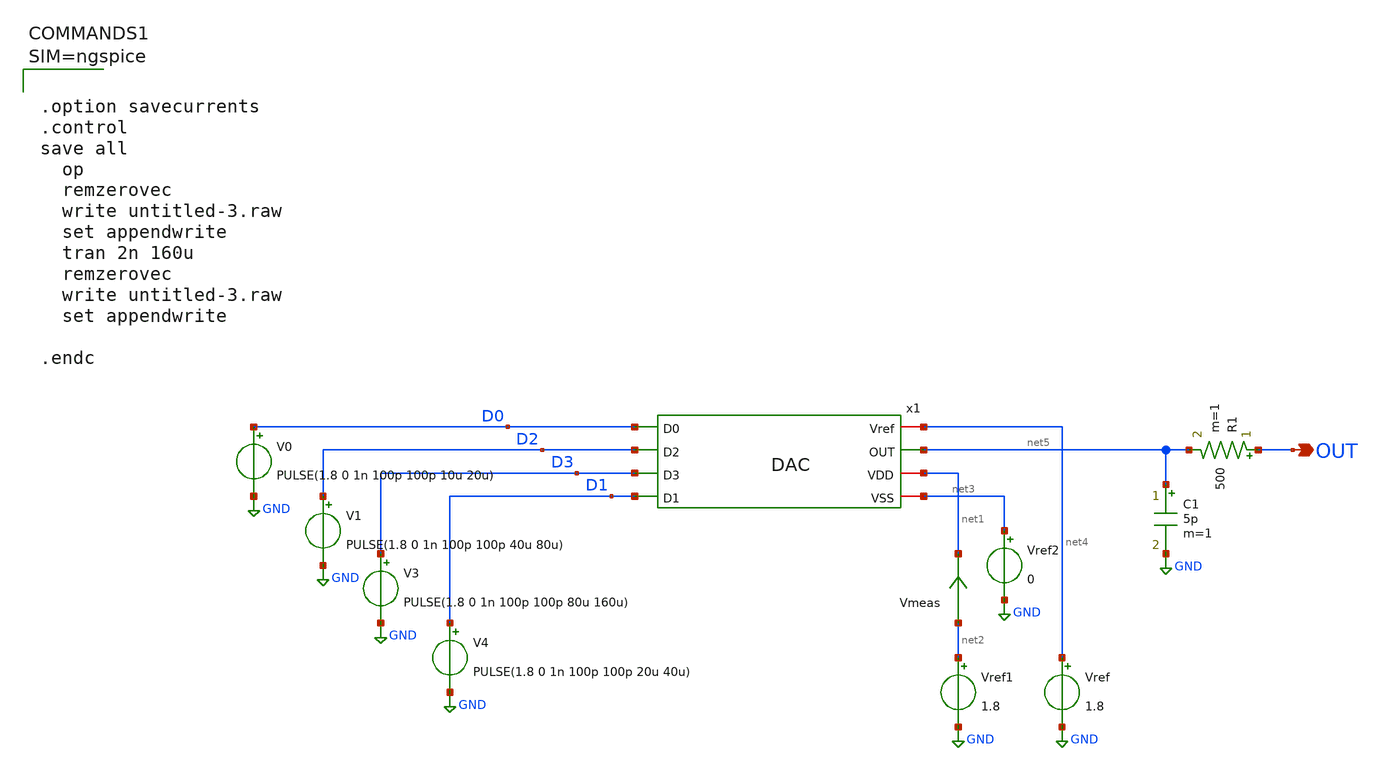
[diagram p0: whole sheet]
** sch_path: tt_um_DAC1/xschem/untiled-3.sch
**.subckt untiled-3 OUT
*.opin OUT
Vref net4 GND 1.8
V0 D0 GND PULSE(1.8 0 1n 100p 100p 10u 20u)
V1 D2 GND PULSE(1.8 0 1n 100p 100p 40u 80u)
V3 D3 GND PULSE(1.8 0 1n 100p 100p 80u 160u)
V4 D1 GND PULSE(1.8 0 1n 100p 100p 20u 40u)
Vref1 net2 GND 1.8
x1 D3 D2 D0 D1 net4 net5 net1 net3 DAC
Vmeas net2 net1 0
.save i(vmeas)
Vref2 net3 GND 0
R1 OUT net5 500 m=1
C1 net5 GND 5p m=1
**** begin user architecture code



.option savecurrents
.control
save all
  op
  remzerovec
  write untitled-3.raw
  set appendwrite
  tran 2n 160u
  remzerovec
  write untitled-3.raw
  set appendwrite

.endc




** opencircuitdesign pdks install
.lib $::SKYWATER_MODELS/sky130.lib.spice tt


**** end user architecture code
**.ends

* expanding   symbol:  DAC.sym # of pins=8
** sym_path: tt_um_DAC1/xschem/DAC.sym
** sch_path: tt_um_DAC1/xschem/DAC.sch
.subckt DAC D3 D2 D0 D1 Vref OUT VDD VSS
*.ipin D0
*.ipin D1
*.ipin D2
*.ipin D3
*.iopin Vref
*.opin OUT
*.iopin VDD
*.iopin VSS
XR3 net5 Vref VSS sky130_fd_pr__res_xhigh_po_0p35 L=16 mult=1 m=1
XR4 G net5 VSS sky130_fd_pr__res_xhigh_po_0p35 L=16 mult=1 m=1
XR5 VDD OUT VSS sky130_fd_pr__res_xhigh_po_0p69 L=1.75 mult=1 m=1
XM6 OUT D0 net4 VSS sky130_fd_pr__nfet_01v8_lvt L=0.18 W=6 nf=3 ad='int((3 + 1)/2) * 6 / 3 * 0.29' as='int((3 + 2)/2) * 6 / 3 * 0.29'
+ pd='2*int((3 + 1)/2) * (6 / 3 + 0.29)' ps='2*int((3 + 2)/2) * (6 / 3 + 0.29)' nrd='0.29 / 6 ' nrs='0.29 / 6 '
+ sa=0 sb=0 sd=0 mult=1 m=1
XM1 OUT D1 net1 VSS sky130_fd_pr__nfet_01v8_lvt L=0.18 W=6 nf=3 ad='int((3 + 1)/2) * 6 / 3 * 0.29' as='int((3 + 2)/2) * 6 / 3 * 0.29'
+ pd='2*int((3 + 1)/2) * (6 / 3 + 0.29)' ps='2*int((3 + 2)/2) * (6 / 3 + 0.29)' nrd='0.29 / 6 ' nrs='0.29 / 6 '
+ sa=0 sb=0 sd=0 mult=1 m=1
XM2 OUT D2 net2 VSS sky130_fd_pr__nfet_01v8_lvt L=0.18 W=6 nf=3 ad='int((3 + 1)/2) * 6 / 3 * 0.29' as='int((3 + 2)/2) * 6 / 3 * 0.29'
+ pd='2*int((3 + 1)/2) * (6 / 3 + 0.29)' ps='2*int((3 + 2)/2) * (6 / 3 + 0.29)' nrd='0.29 / 6 ' nrs='0.29 / 6 '
+ sa=0 sb=0 sd=0 mult=1 m=1
XM3 OUT D3 net3 VSS sky130_fd_pr__nfet_01v8_lvt L=0.18 W=6 nf=3 ad='int((3 + 1)/2) * 6 / 3 * 0.29' as='int((3 + 2)/2) * 6 / 3 * 0.29'
+ pd='2*int((3 + 1)/2) * (6 / 3 + 0.29)' ps='2*int((3 + 2)/2) * (6 / 3 + 0.29)' nrd='0.29 / 6 ' nrs='0.29 / 6 '
+ sa=0 sb=0 sd=0 mult=1 m=1
XM4 G G VSS VSS sky130_fd_pr__nfet_01v8_lvt L=0.18 W=8 nf=3 ad='int((3 + 1)/2) * 8 / 3 * 0.29' as='int((3 + 2)/2) * 8 / 3 * 0.29'
+ pd='2*int((3 + 1)/2) * (8 / 3 + 0.29)' ps='2*int((3 + 2)/2) * (8 / 3 + 0.29)' nrd='0.29 / 8 ' nrs='0.29 / 8 '
+ sa=0 sb=0 sd=0 mult=1 m=1
XM5 net4 G VSS VSS sky130_fd_pr__nfet_01v8_lvt L=0.18 W=8 nf=3 ad='int((3 + 1)/2) * 8 / 3 * 0.29' as='int((3 + 2)/2) * 8 / 3 * 0.29'
+ pd='2*int((3 + 1)/2) * (8 / 3 + 0.29)' ps='2*int((3 + 2)/2) * (8 / 3 + 0.29)' nrd='0.29 / 8 ' nrs='0.29 / 8 '
+ sa=0 sb=0 sd=0 mult=1 m=1
XM7 net1 G VSS VSS sky130_fd_pr__nfet_01v8_lvt L=0.18 W=16 nf=6 ad='int((6 + 1)/2) * 16 / 6 * 0.29' as='int((6 + 2)/2) * 16 / 6 * 0.29'
+ pd='2*int((6 + 1)/2) * (16 / 6 + 0.29)' ps='2*int((6 + 2)/2) * (16 / 6 + 0.29)' nrd='0.29 / 16 ' nrs='0.29 / 16 '
+ sa=0 sb=0 sd=0 mult=1 m=1
XM8 net2 G VSS VSS sky130_fd_pr__nfet_01v8_lvt L=0.18 W=33 nf=12 ad='int((12 + 1)/2) * 33 / 12 * 0.29'
+ as='int((12 + 2)/2) * 33 / 12 * 0.29' pd='2*int((12 + 1)/2) * (33 / 12 + 0.29)' ps='2*int((12 + 2)/2) * (33 / 12 + 0.29)'
+ nrd='0.29 / 33 ' nrs='0.29 / 33 ' sa=0 sb=0 sd=0 mult=1 m=1
XM9 net3 G VSS VSS sky130_fd_pr__nfet_01v8_lvt L=0.18 W=69 nf=24 ad='int((24 + 1)/2) * 69 / 24 * 0.29'
+ as='int((24 + 2)/2) * 69 / 24 * 0.29' pd='2*int((24 + 1)/2) * (69 / 24 + 0.29)' ps='2*int((24 + 2)/2) * (69 / 24 + 0.29)'
+ nrd='0.29 / 69 ' nrs='0.29 / 69 ' sa=0 sb=0 sd=0 mult=1 m=1
.ends

.GLOBAL GND
.end
